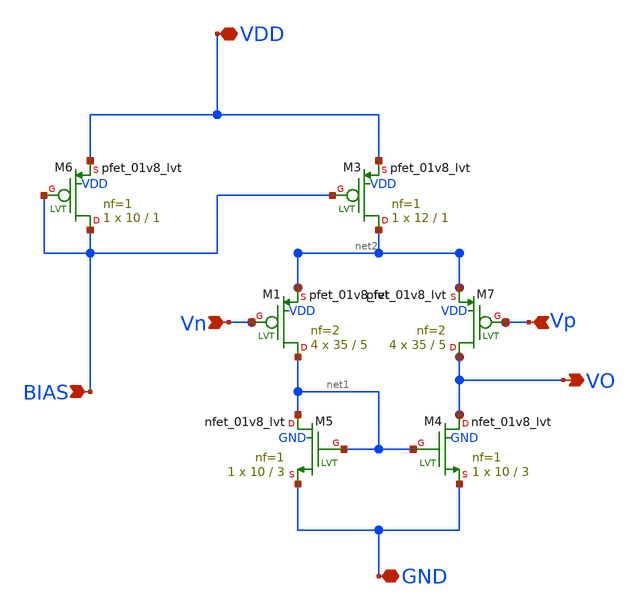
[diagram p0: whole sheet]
** sch_path: examples/two_stage_opamp/xschem/two_stage_opamp.sch
**.subckt two_stage_opamp GND BIAS Vp Vn VO VDD
*.iopin GND
*.ipin BIAS
*.ipin Vp
*.ipin Vn
*.opin VO
*.iopin VDD
XM3 net2 BIAS VDD VDD sky130_fd_pr__pfet_01v8_lvt L=1 W=12 nf=1 ad='int((1 + 1)/2) * 12 / 1 * 0.29' as='int((1 + 2)/2) * 12 / 1 * 0.29'
+ pd='2*int((1 + 1)/2) * (12 / 1 + 0.29)' ps='2*int((1 + 2)/2) * (12 / 1 + 0.29)' nrd='0.29 / 12 ' nrs='0.29 / 12 '
+ sa=0 sb=0 sd=0 mult=1 m=1
XM4 VO net1 GND GND sky130_fd_pr__nfet_01v8_lvt L=3 W=10 nf=1 ad='int((1 + 1)/2) * 10 / 1 * 0.29' as='int((1 + 2)/2) * 10 / 1 * 0.29'
+ pd='2*int((1 + 1)/2) * (10 / 1 + 0.29)' ps='2*int((1 + 2)/2) * (10 / 1 + 0.29)' nrd='0.29 / 10 ' nrs='0.29 / 10 '
+ sa=0 sb=0 sd=0 mult=1 m=1
XM5 net1 net1 GND GND sky130_fd_pr__nfet_01v8_lvt L=3 W=10 nf=1 ad='int((1 + 1)/2) * 10 / 1 * 0.29' as='int((1 + 2)/2) * 10 / 1 * 0.29'
+ pd='2*int((1 + 1)/2) * (10 / 1 + 0.29)' ps='2*int((1 + 2)/2) * (10 / 1 + 0.29)' nrd='0.29 / 10 ' nrs='0.29 / 10 '
+ sa=0 sb=0 sd=0 mult=1 m=1
XM6 BIAS BIAS VDD VDD sky130_fd_pr__pfet_01v8_lvt L=1 W=10 nf=1 ad='int((1 + 1)/2) * 10 / 1 * 0.29' as='int((1 + 2)/2) * 10 / 1 * 0.29'
+ pd='2*int((1 + 1)/2) * (10 / 1 + 0.29)' ps='2*int((1 + 2)/2) * (10 / 1 + 0.29)' nrd='0.29 / 10 ' nrs='0.29 / 10 '
+ sa=0 sb=0 sd=0 mult=1 m=1
XM1 net1 Vn net2 VDD sky130_fd_pr__pfet_01v8_lvt L=5 W=35 nf=2 ad='int((2 + 1)/2) * 35 / 2 * 0.29' as='int((2 + 2)/2) * 35 / 2 * 0.29'
+ pd='2*int((2 + 1)/2) * (35 / 2 + 0.29)' ps='2*int((2 + 2)/2) * (35 / 2 + 0.29)' nrd='0.29 / 35 ' nrs='0.29 / 35 '
+ sa=0 sb=0 sd=0 mult=4 m=4
XM7 VO Vp net2 VDD sky130_fd_pr__pfet_01v8_lvt L=5 W=35 nf=2 ad='int((2 + 1)/2) * 35 / 2 * 0.29' as='int((2 + 2)/2) * 35 / 2 * 0.29'
+ pd='2*int((2 + 1)/2) * (35 / 2 + 0.29)' ps='2*int((2 + 2)/2) * (35 / 2 + 0.29)' nrd='0.29 / 35 ' nrs='0.29 / 35 '
+ sa=0 sb=0 sd=0 mult=4 m=4
**.ends
.end
